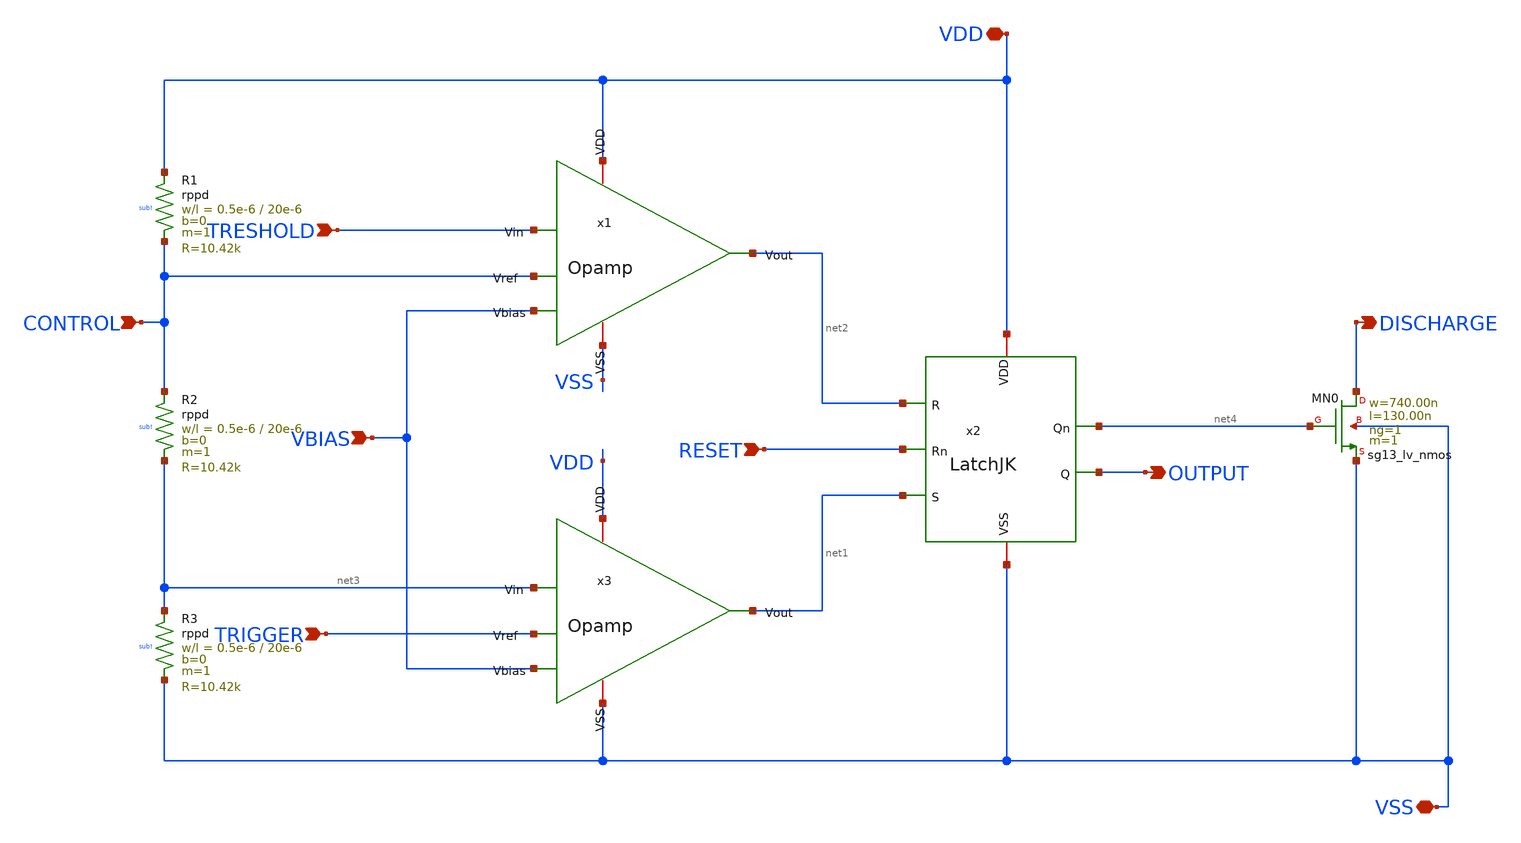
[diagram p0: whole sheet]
** sch_path: xschem/555.sch
**.subckt 555 OUTPUT TRIGGER VDD VSS RESET TRESHOLD DISCHARGE VBIAS CONTROL
*.opin OUTPUT
*.ipin TRIGGER
*.iopin VDD
*.iopin VSS
*.ipin RESET
*.ipin TRESHOLD
*.opin DISCHARGE
*.ipin VBIAS
*.ipin CONTROL
x1 VDD TRESHOLD CONTROL net2 VBIAS VSS Opamp
x2 VDD net1 net4 OUTPUT net2 RESET VSS LatchJK
x3 VDD net3 TRIGGER net1 VBIAS VSS Opamp
XR1 VDD CONTROL sub! rppd w=0.5e-6 l=20e-6 m=1 b=0 mm_ok=1
XR2 CONTROL net3 sub! rppd w=0.5e-6 l=20e-6 m=1 b=0 mm_ok=1
XR3 net3 VSS sub! rppd w=0.5e-6 l=20e-6 m=1 b=0 mm_ok=1
XMN0 DISCHARGE net4 VSS VSS sg13_lv_nmos w=740.00n l=130.00n ng=1 m=1 mm_ok=1
**.ends
.end
